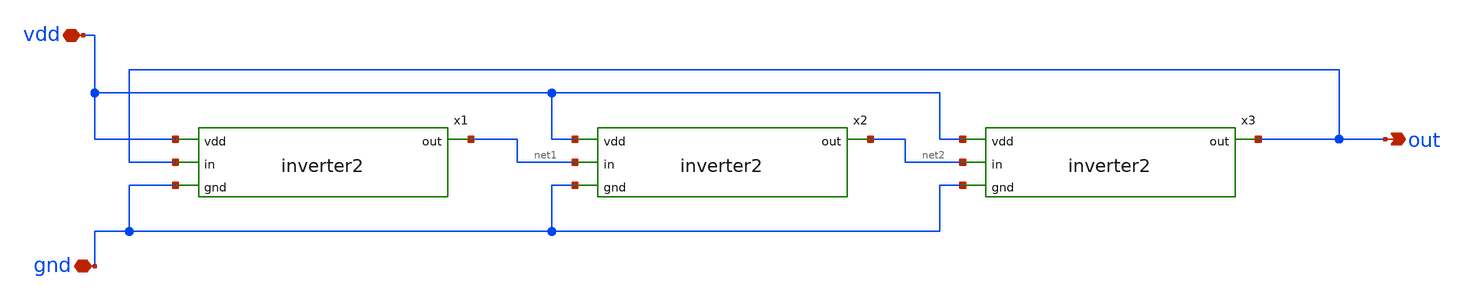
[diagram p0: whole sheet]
** sch_path: icdec_ringoscillator/ringoscillator.sch
**.subckt ringoscillator vdd gnd out
*.iopin vdd
*.iopin gnd
*.opin out
x1 vdd out net1 gnd inverter2
x2 vdd net1 net2 gnd inverter2
x3 vdd net2 out gnd inverter2
**.ends

* expanding   symbol:  /home/muhammadkhairulfattah/icdec_inverter2/inverter2.sym # of pins=4
** sym_path: icdec_inverter2/inverter2.sym
** sch_path: icdec_inverter2/inverter2.sch
.subckt inverter2 vdd in out gnd
*.opin out
*.ipin vdd
*.ipin in
*.ipin gnd
XM1 out in gnd gnd sky130_fd_pr__nfet_01v8 L=0.15 W=1 nf=1 ad='int((nf+1)/2) * W/nf * 0.29' as='int((nf+2)/2) * W/nf * 0.29'
+ pd='2*int((nf+1)/2) * (W/nf + 0.29)' ps='2*int((nf+2)/2) * (W/nf + 0.29)' nrd='0.29 / W' nrs='0.29 / W'
+ sa=0 sb=0 sd=0 mult=1 m=1
XM2 out in vdd vdd sky130_fd_pr__pfet_01v8 L=0.15 W=1 nf=1 ad='int((nf+1)/2) * W/nf * 0.29' as='int((nf+2)/2) * W/nf * 0.29'
+ pd='2*int((nf+1)/2) * (W/nf + 0.29)' ps='2*int((nf+2)/2) * (W/nf + 0.29)' nrd='0.29 / W' nrs='0.29 / W'
+ sa=0 sb=0 sd=0 mult=1 m=1
.ends

.end
